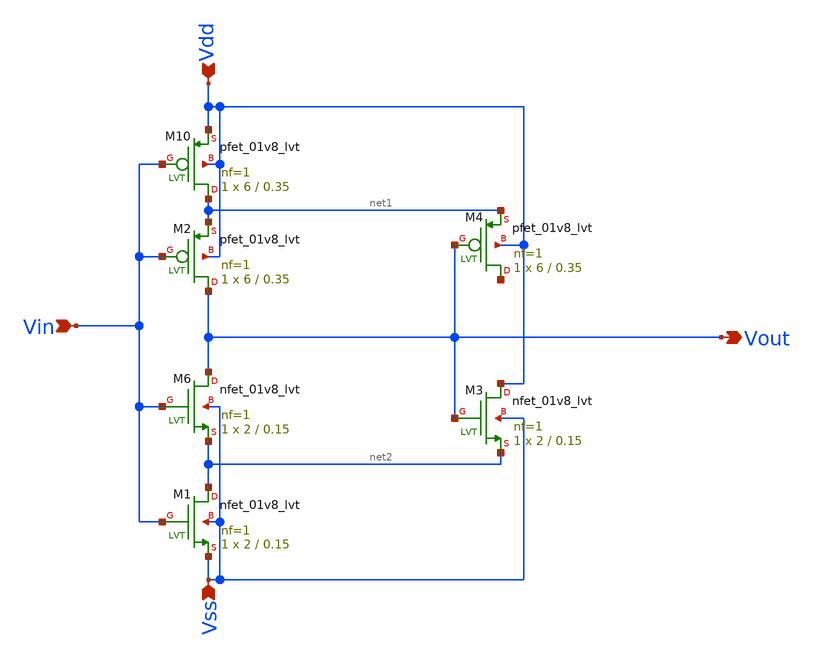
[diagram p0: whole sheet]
** sch_path: custom_gds/tt_um_test_commit/xschem/schmitt_trigger_ro.sch
**.subckt schmitt_trigger_ro Vdd Vss Vin Vout
*.ipin Vdd
*.ipin Vss
*.ipin Vin
*.opin Vout
XM10 net1 Vin Vdd Vdd sky130_fd_pr__pfet_01v8_lvt L=0.35 W=6 nf=1 ad='int((1 + 1)/2) * 6 / 1 * 0.29'
+ as='int((1 + 2)/2) * 6 / 1 * 0.29' pd='2*int((1 + 1)/2) * (6 / 1 + 0.29)' ps='2*int((1 + 2)/2) * (6 / 1 + 0.29)'
+ nrd='0.29 / 6 ' nrs='0.29 / 6 ' sa=0 sb=0 sd=0 mult=1 m=1
XM2 Vout Vin net1 Vdd sky130_fd_pr__pfet_01v8_lvt L=0.35 W=6 nf=1 ad='int((1 + 1)/2) * 6 / 1 * 0.29'
+ as='int((1 + 2)/2) * 6 / 1 * 0.29' pd='2*int((1 + 1)/2) * (6 / 1 + 0.29)' ps='2*int((1 + 2)/2) * (6 / 1 + 0.29)'
+ nrd='0.29 / 6 ' nrs='0.29 / 6 ' sa=0 sb=0 sd=0 mult=1 m=1
XM4 net3 Vout net1 Vdd sky130_fd_pr__pfet_01v8_lvt L=0.35 W=6 nf=1 ad='int((1 + 1)/2) * 6 / 1 * 0.29'
+ as='int((1 + 2)/2) * 6 / 1 * 0.29' pd='2*int((1 + 1)/2) * (6 / 1 + 0.29)' ps='2*int((1 + 2)/2) * (6 / 1 + 0.29)'
+ nrd='0.29 / 6 ' nrs='0.29 / 6 ' sa=0 sb=0 sd=0 mult=1 m=1
XM6 Vout Vin net2 Vss sky130_fd_pr__nfet_01v8_lvt L=0.15 W=2 nf=1 ad='int((1 + 1)/2) * 2 / 1 * 0.29'
+ as='int((1 + 2)/2) * 2 / 1 * 0.29' pd='2*int((1 + 1)/2) * (2 / 1 + 0.29)' ps='2*int((1 + 2)/2) * (2 / 1 + 0.29)'
+ nrd='0.29 / 2 ' nrs='0.29 / 2 ' sa=0 sb=0 sd=0 mult=1 m=1
XM1 net2 Vin Vss Vss sky130_fd_pr__nfet_01v8_lvt L=0.15 W=2 nf=1 ad='int((1 + 1)/2) * 2 / 1 * 0.29' as='int((1 + 2)/2) * 2 / 1 * 0.29'
+ pd='2*int((1 + 1)/2) * (2 / 1 + 0.29)' ps='2*int((1 + 2)/2) * (2 / 1 + 0.29)' nrd='0.29 / 2 ' nrs='0.29 / 2 '
+ sa=0 sb=0 sd=0 mult=1 m=1
XM3 Vdd Vout net2 Vss sky130_fd_pr__nfet_01v8_lvt L=0.15 W=2 nf=1 ad='int((1 + 1)/2) * 2 / 1 * 0.29'
+ as='int((1 + 2)/2) * 2 / 1 * 0.29' pd='2*int((1 + 1)/2) * (2 / 1 + 0.29)' ps='2*int((1 + 2)/2) * (2 / 1 + 0.29)'
+ nrd='0.29 / 2 ' nrs='0.29 / 2 ' sa=0 sb=0 sd=0 mult=1 m=1
**.ends
.end
